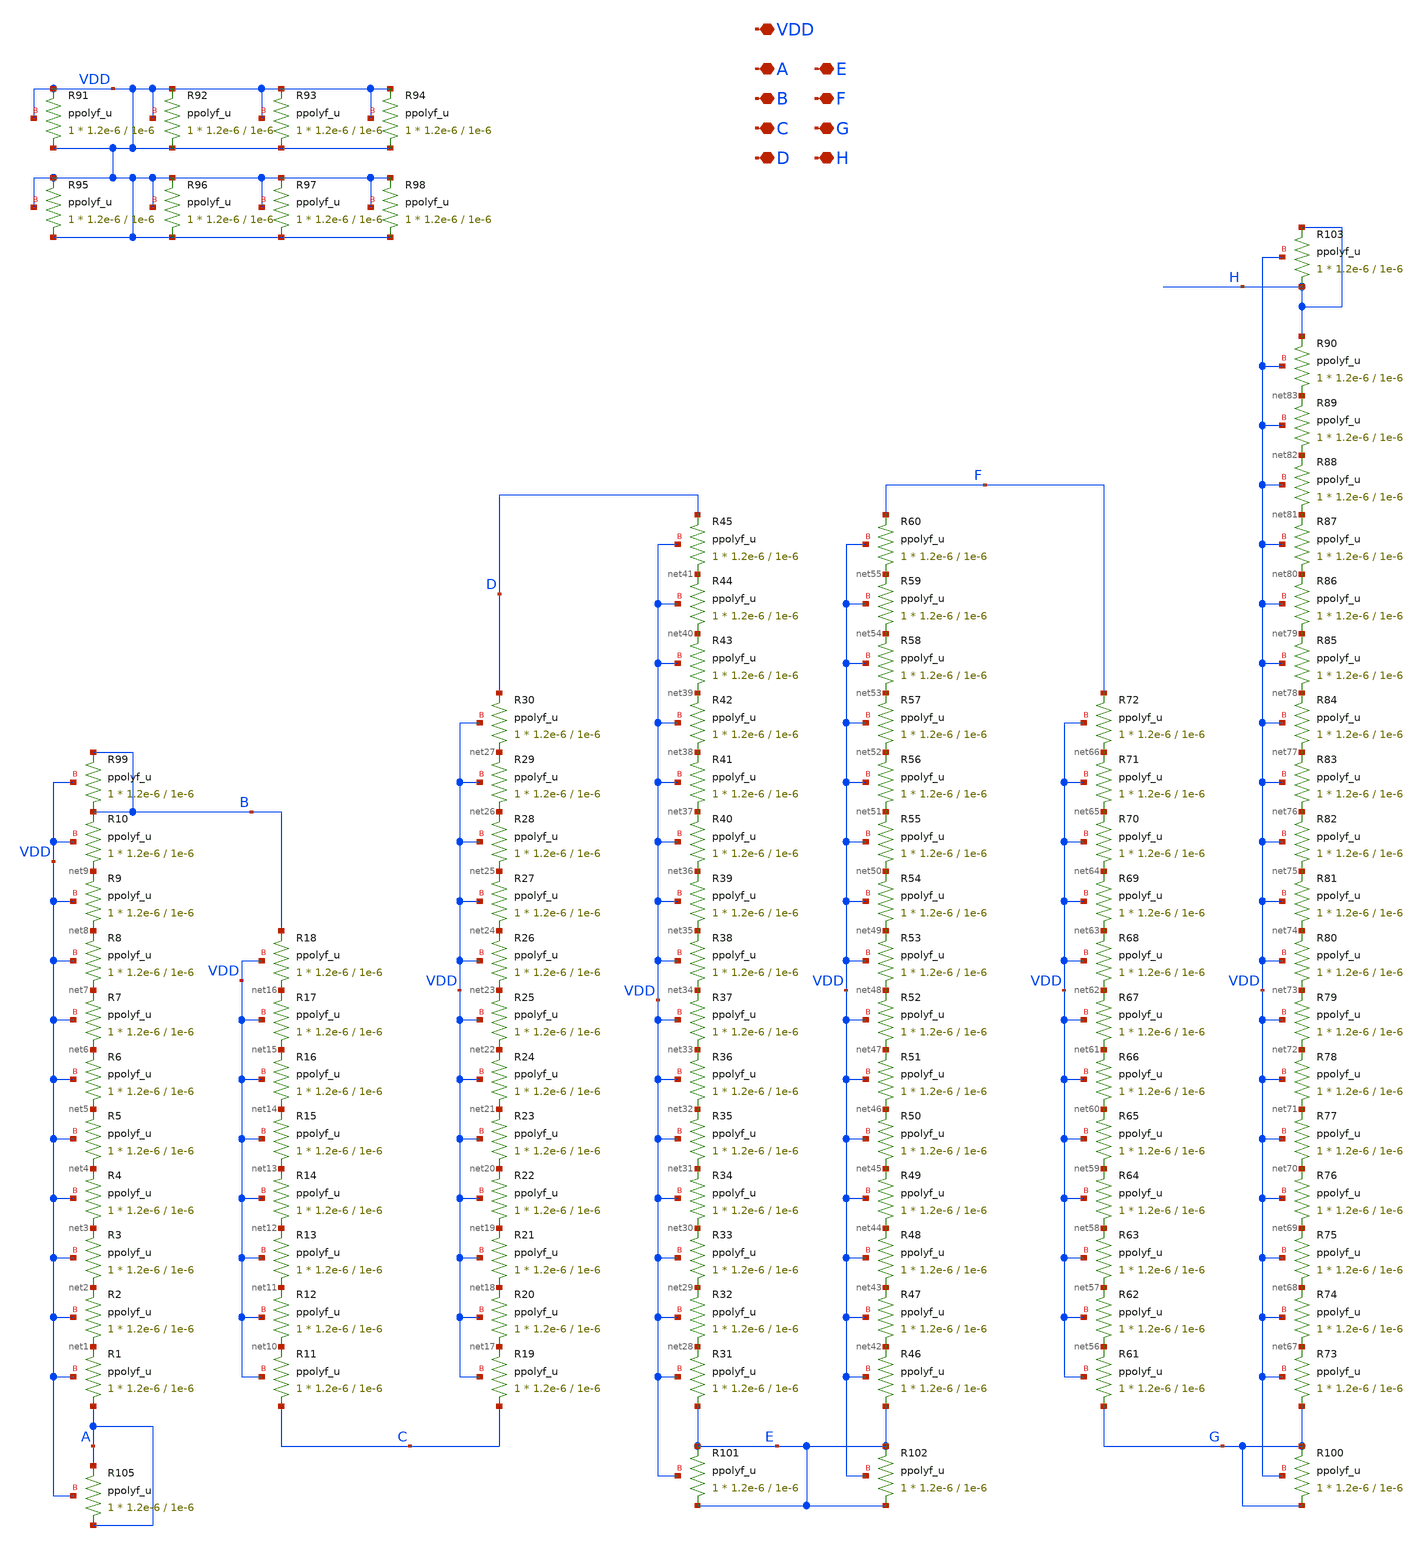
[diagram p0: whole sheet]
** sch_path: SCOP_INPUT_AND_MUX_PAKISTAN_03/Xschem/PGA_block_new/resis_PGA.sch
**.subckt resis_PGA VDD A B C D E F G H
*.iopin VDD
*.iopin A
*.iopin B
*.iopin C
*.iopin D
*.iopin E
*.iopin F
*.iopin G
*.iopin H
XR1 A net1 VDD ppolyf_u r_width=1.2e-6 r_length=1e-6 m=1
XR2 net1 net2 VDD ppolyf_u r_width=1.2e-6 r_length=1e-6 m=1
XR3 net2 net3 VDD ppolyf_u r_width=1.2e-6 r_length=1e-6 m=1
XR4 net3 net4 VDD ppolyf_u r_width=1.2e-6 r_length=1e-6 m=1
XR5 net4 net5 VDD ppolyf_u r_width=1.2e-6 r_length=1e-6 m=1
XR6 net5 net6 VDD ppolyf_u r_width=1.2e-6 r_length=1e-6 m=1
XR7 net6 net7 VDD ppolyf_u r_width=1.2e-6 r_length=1e-6 m=1
XR8 net7 net8 VDD ppolyf_u r_width=1.2e-6 r_length=1e-6 m=1
XR9 net8 net9 VDD ppolyf_u r_width=1.2e-6 r_length=1e-6 m=1
XR10 net9 B VDD ppolyf_u r_width=1.2e-6 r_length=1e-6 m=1
XR11 C net10 VDD ppolyf_u r_width=1.2e-6 r_length=1e-6 m=1
XR12 net10 net11 VDD ppolyf_u r_width=1.2e-6 r_length=1e-6 m=1
XR13 net11 net12 VDD ppolyf_u r_width=1.2e-6 r_length=1e-6 m=1
XR14 net12 net13 VDD ppolyf_u r_width=1.2e-6 r_length=1e-6 m=1
XR15 net13 net14 VDD ppolyf_u r_width=1.2e-6 r_length=1e-6 m=1
XR16 net14 net15 VDD ppolyf_u r_width=1.2e-6 r_length=1e-6 m=1
XR17 net15 net16 VDD ppolyf_u r_width=1.2e-6 r_length=1e-6 m=1
XR18 net16 B VDD ppolyf_u r_width=1.2e-6 r_length=1e-6 m=1
XR19 C net17 VDD ppolyf_u r_width=1.2e-6 r_length=1e-6 m=1
XR20 net17 net18 VDD ppolyf_u r_width=1.2e-6 r_length=1e-6 m=1
XR21 net18 net19 VDD ppolyf_u r_width=1.2e-6 r_length=1e-6 m=1
XR22 net19 net20 VDD ppolyf_u r_width=1.2e-6 r_length=1e-6 m=1
XR23 net20 net21 VDD ppolyf_u r_width=1.2e-6 r_length=1e-6 m=1
XR24 net21 net22 VDD ppolyf_u r_width=1.2e-6 r_length=1e-6 m=1
XR25 net22 net23 VDD ppolyf_u r_width=1.2e-6 r_length=1e-6 m=1
XR26 net23 net24 VDD ppolyf_u r_width=1.2e-6 r_length=1e-6 m=1
XR27 net24 net25 VDD ppolyf_u r_width=1.2e-6 r_length=1e-6 m=1
XR28 net25 net26 VDD ppolyf_u r_width=1.2e-6 r_length=1e-6 m=1
XR29 net26 net27 VDD ppolyf_u r_width=1.2e-6 r_length=1e-6 m=1
XR30 net27 D VDD ppolyf_u r_width=1.2e-6 r_length=1e-6 m=1
XR31 E net28 VDD ppolyf_u r_width=1.2e-6 r_length=1e-6 m=1
XR32 net28 net29 VDD ppolyf_u r_width=1.2e-6 r_length=1e-6 m=1
XR33 net29 net30 VDD ppolyf_u r_width=1.2e-6 r_length=1e-6 m=1
XR34 net30 net31 VDD ppolyf_u r_width=1.2e-6 r_length=1e-6 m=1
XR35 net31 net32 VDD ppolyf_u r_width=1.2e-6 r_length=1e-6 m=1
XR36 net32 net33 VDD ppolyf_u r_width=1.2e-6 r_length=1e-6 m=1
XR37 net33 net34 VDD ppolyf_u r_width=1.2e-6 r_length=1e-6 m=1
XR38 net34 net35 VDD ppolyf_u r_width=1.2e-6 r_length=1e-6 m=1
XR39 net35 net36 VDD ppolyf_u r_width=1.2e-6 r_length=1e-6 m=1
XR40 net36 net37 VDD ppolyf_u r_width=1.2e-6 r_length=1e-6 m=1
XR41 net37 net38 VDD ppolyf_u r_width=1.2e-6 r_length=1e-6 m=1
XR42 net38 net39 VDD ppolyf_u r_width=1.2e-6 r_length=1e-6 m=1
XR43 net39 net40 VDD ppolyf_u r_width=1.2e-6 r_length=1e-6 m=1
XR44 net40 net41 VDD ppolyf_u r_width=1.2e-6 r_length=1e-6 m=1
XR45 net41 D VDD ppolyf_u r_width=1.2e-6 r_length=1e-6 m=1
XR46 E net42 VDD ppolyf_u r_width=1.2e-6 r_length=1e-6 m=1
XR47 net42 net43 VDD ppolyf_u r_width=1.2e-6 r_length=1e-6 m=1
XR48 net43 net44 VDD ppolyf_u r_width=1.2e-6 r_length=1e-6 m=1
XR49 net44 net45 VDD ppolyf_u r_width=1.2e-6 r_length=1e-6 m=1
XR50 net45 net46 VDD ppolyf_u r_width=1.2e-6 r_length=1e-6 m=1
XR51 net46 net47 VDD ppolyf_u r_width=1.2e-6 r_length=1e-6 m=1
XR52 net47 net48 VDD ppolyf_u r_width=1.2e-6 r_length=1e-6 m=1
XR53 net48 net49 VDD ppolyf_u r_width=1.2e-6 r_length=1e-6 m=1
XR54 net49 net50 VDD ppolyf_u r_width=1.2e-6 r_length=1e-6 m=1
XR55 net50 net51 VDD ppolyf_u r_width=1.2e-6 r_length=1e-6 m=1
XR56 net51 net52 VDD ppolyf_u r_width=1.2e-6 r_length=1e-6 m=1
XR57 net52 net53 VDD ppolyf_u r_width=1.2e-6 r_length=1e-6 m=1
XR58 net53 net54 VDD ppolyf_u r_width=1.2e-6 r_length=1e-6 m=1
XR59 net54 net55 VDD ppolyf_u r_width=1.2e-6 r_length=1e-6 m=1
XR60 net55 F VDD ppolyf_u r_width=1.2e-6 r_length=1e-6 m=1
XR61 G net56 VDD ppolyf_u r_width=1.2e-6 r_length=1e-6 m=1
XR62 net56 net57 VDD ppolyf_u r_width=1.2e-6 r_length=1e-6 m=1
XR63 net57 net58 VDD ppolyf_u r_width=1.2e-6 r_length=1e-6 m=1
XR64 net58 net59 VDD ppolyf_u r_width=1.2e-6 r_length=1e-6 m=1
XR65 net59 net60 VDD ppolyf_u r_width=1.2e-6 r_length=1e-6 m=1
XR66 net60 net61 VDD ppolyf_u r_width=1.2e-6 r_length=1e-6 m=1
XR67 net61 net62 VDD ppolyf_u r_width=1.2e-6 r_length=1e-6 m=1
XR68 net62 net63 VDD ppolyf_u r_width=1.2e-6 r_length=1e-6 m=1
XR69 net63 net64 VDD ppolyf_u r_width=1.2e-6 r_length=1e-6 m=1
XR70 net64 net65 VDD ppolyf_u r_width=1.2e-6 r_length=1e-6 m=1
XR71 net65 net66 VDD ppolyf_u r_width=1.2e-6 r_length=1e-6 m=1
XR72 net66 F VDD ppolyf_u r_width=1.2e-6 r_length=1e-6 m=1
XR73 G net67 VDD ppolyf_u r_width=1.2e-6 r_length=1e-6 m=1
XR74 net67 net68 VDD ppolyf_u r_width=1.2e-6 r_length=1e-6 m=1
XR75 net68 net69 VDD ppolyf_u r_width=1.2e-6 r_length=1e-6 m=1
XR76 net69 net70 VDD ppolyf_u r_width=1.2e-6 r_length=1e-6 m=1
XR77 net70 net71 VDD ppolyf_u r_width=1.2e-6 r_length=1e-6 m=1
XR78 net71 net72 VDD ppolyf_u r_width=1.2e-6 r_length=1e-6 m=1
XR79 net72 net73 VDD ppolyf_u r_width=1.2e-6 r_length=1e-6 m=1
XR80 net73 net74 VDD ppolyf_u r_width=1.2e-6 r_length=1e-6 m=1
XR81 net74 net75 VDD ppolyf_u r_width=1.2e-6 r_length=1e-6 m=1
XR82 net75 net76 VDD ppolyf_u r_width=1.2e-6 r_length=1e-6 m=1
XR83 net76 net77 VDD ppolyf_u r_width=1.2e-6 r_length=1e-6 m=1
XR84 net77 net78 VDD ppolyf_u r_width=1.2e-6 r_length=1e-6 m=1
XR85 net78 net79 VDD ppolyf_u r_width=1.2e-6 r_length=1e-6 m=1
XR86 net79 net80 VDD ppolyf_u r_width=1.2e-6 r_length=1e-6 m=1
XR87 net80 net81 VDD ppolyf_u r_width=1.2e-6 r_length=1e-6 m=1
XR88 net81 net82 VDD ppolyf_u r_width=1.2e-6 r_length=1e-6 m=1
XR89 net82 net83 VDD ppolyf_u r_width=1.2e-6 r_length=1e-6 m=1
XR90 net83 H VDD ppolyf_u r_width=1.2e-6 r_length=1e-6 m=1
XR91 VDD VDD VDD ppolyf_u r_width=1.2e-6 r_length=1e-6 m=1
XR92 VDD VDD VDD ppolyf_u r_width=1.2e-6 r_length=1e-6 m=1
XR93 VDD VDD VDD ppolyf_u r_width=1.2e-6 r_length=1e-6 m=1
XR94 VDD VDD VDD ppolyf_u r_width=1.2e-6 r_length=1e-6 m=1
XR95 VDD VDD VDD ppolyf_u r_width=1.2e-6 r_length=1e-6 m=1
XR96 VDD VDD VDD ppolyf_u r_width=1.2e-6 r_length=1e-6 m=1
XR97 VDD VDD VDD ppolyf_u r_width=1.2e-6 r_length=1e-6 m=1
XR98 VDD VDD VDD ppolyf_u r_width=1.2e-6 r_length=1e-6 m=1
XR99 B B VDD ppolyf_u r_width=1.2e-6 r_length=1e-6 m=1
XR103 H H VDD ppolyf_u r_width=1.2e-6 r_length=1e-6 m=1
XR105 A A VDD ppolyf_u r_width=1.2e-6 r_length=1e-6 m=1
XR100 G G VDD ppolyf_u r_width=1.2e-6 r_length=1e-6 m=1
XR101 E E VDD ppolyf_u r_width=1.2e-6 r_length=1e-6 m=1
XR102 E E VDD ppolyf_u r_width=1.2e-6 r_length=1e-6 m=1
**.ends
.end
